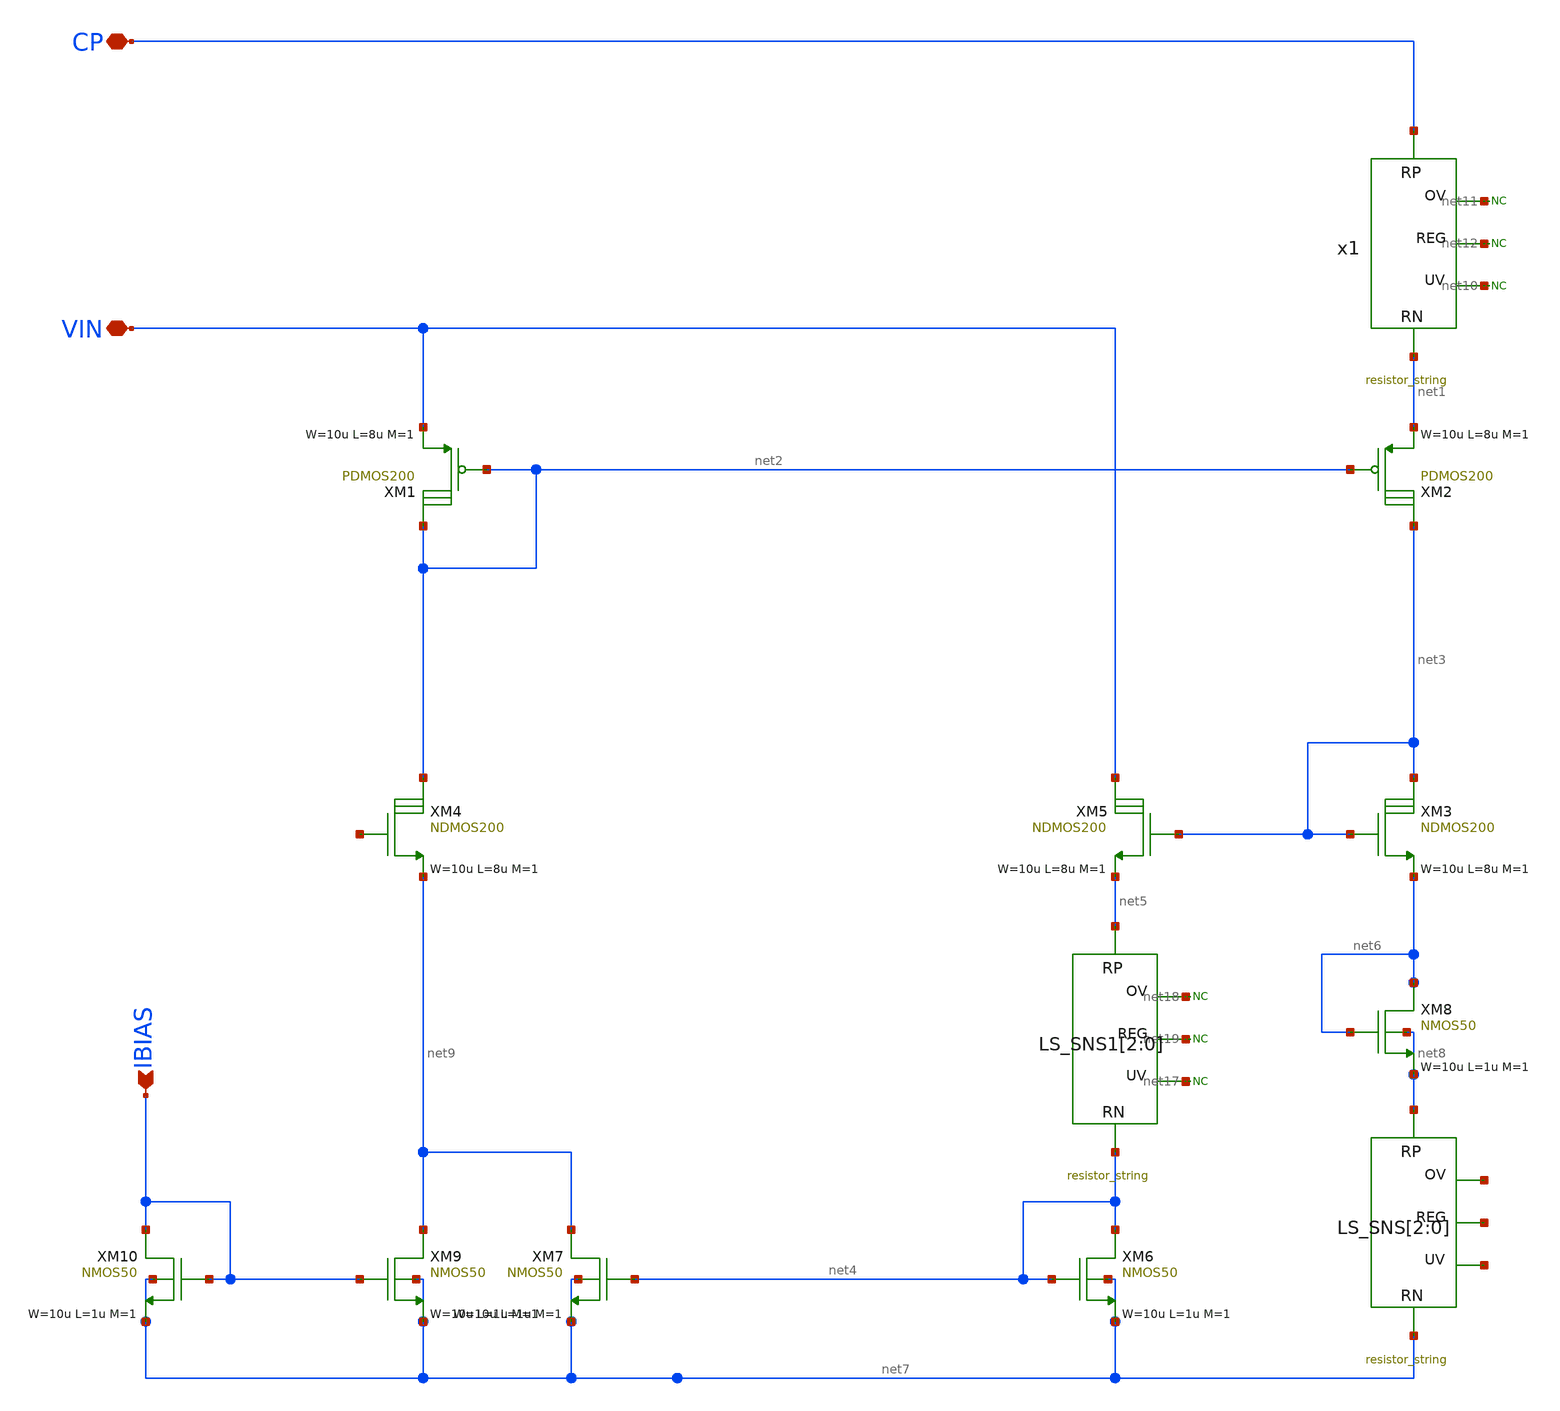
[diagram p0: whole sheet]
** sch_path: xschem/designs/CP_VoltageMonitor.sch
**.subckt CP_VoltageMonitor CP VIN IBIAS
*.iopin CP
*.iopin VIN
*.ipin IBIAS
x1 CP net1 net10 net11 net12 resistor_string
XM1 net2 net2 VIN PDMOS200 W=10u L=8u M=1 MM_SIGMA=0
XM2 net3 net2 net1 PDMOS200 W=10u L=8u M=1 MM_SIGMA=0
* noconn #net10
* noconn #net12
* noconn #net11
XM3 net3 net3 net6 NDMOS200 W=10u L=8u M=1 MM_SIGMA=0
LS_SNS[2] net8 net7 net13[2] net14[2] net15[2] resistor_string
LS_SNS[1] net8 net7 net13[1] net14[1] net15[1] resistor_string
LS_SNS[0] net8 net7 net13[0] net14[0] net15[0] resistor_string
XM4 net2 net16 net9 NDMOS200 W=10u L=8u M=1 MM_SIGMA=0
XM5 VIN net3 net5 NDMOS200 W=10u L=8u M=1 MM_SIGMA=0
LS_SNS1[2] net5 net4 net17 net18 net19 resistor_string
LS_SNS1[1] net5 net4 net17 net18 net19 resistor_string
LS_SNS1[0] net5 net4 net17 net18 net19 resistor_string
* noconn #net18
* noconn #net19
* noconn #net17
XM6 net4 net4 net7 net7 NMOS50 W=10u L=1u M=1 MM_SIGMA=0
XM8 net6 net6 net8 net8 NMOS50 W=10u L=1u M=1 MM_SIGMA=0
XM7 net9 net4 net7 net7 NMOS50 W=10u L=1u M=1 MM_SIGMA=0
XM9 net9 IBIAS net7 net7 NMOS50 W=10u L=1u M=1 MM_SIGMA=0
XM10 IBIAS IBIAS net7 net7 NMOS50 W=10u L=1u M=1 MM_SIGMA=0
**.ends

* expanding   symbol:  designs/resistor_string.sym # of pins=5
** sym_path: xschem/designs/resistor_string.sym
** sch_path: xschem/designs/resistor_string.sch
.subckt resistor_string RP RN UV OV REG
*.iopin RP
*.iopin RN
*.iopin OV
*.iopin REG
*.iopin UV
XR1 RP net1 RPOLY_HI L=10u W=2u MM_SIGMA=0
XR2 net1 net2 RPOLY_HI L=10u W=2u MM_SIGMA=0
XR3 net2 net3 RPOLY_HI L=10u W=2u MM_SIGMA=0
XR4 net3 net4 RPOLY_HI L=10u W=2u MM_SIGMA=0
XR5 net4 OV RPOLY_HI L=10u W=2u MM_SIGMA=0
XR6 OV net5 RPOLY_HI L=10u W=2u MM_SIGMA=0
XR7 net5 net6 RPOLY_HI L=10u W=2u MM_SIGMA=0
XR8 net6 net7 RPOLY_HI L=10u W=2u MM_SIGMA=0
XR9 net7 net8 RPOLY_HI L=10u W=2u MM_SIGMA=0
XR10 net8 net9 RPOLY_HI L=10u W=2u MM_SIGMA=0
XR11 net9 net10 RPOLY_HI L=10u W=2u MM_SIGMA=0
XR12 net10 net11 RPOLY_HI L=10u W=2u MM_SIGMA=0
XR13 net11 REG RPOLY_HI L=10u W=2u MM_SIGMA=0
XR14 REG net12 RPOLY_HI L=10u W=2u MM_SIGMA=0
XR15 net12 net13 RPOLY_HI L=10u W=2u MM_SIGMA=0
XR16 net13 net14 RPOLY_HI L=10u W=2u MM_SIGMA=0
XR17 net14 net15 RPOLY_HI L=10u W=2u MM_SIGMA=0
XR18 net15 net16 RPOLY_HI L=10u W=2u MM_SIGMA=0
XR19 net16 net17 RPOLY_HI L=10u W=2u MM_SIGMA=0
XR20 net17 UV RPOLY_HI L=10u W=2u MM_SIGMA=0
XR21 UV net18 RPOLY_HI L=10u W=2u MM_SIGMA=0
XR22 net18 net19 RPOLY_HI L=10u W=2u MM_SIGMA=0
XR23 net19 net20 RPOLY_HI L=10u W=2u MM_SIGMA=0
XR24 net20 net21 RPOLY_HI L=10u W=2u MM_SIGMA=0
XR25 net21 RN RPOLY_HI L=10u W=2u MM_SIGMA=0
.ends

.end
